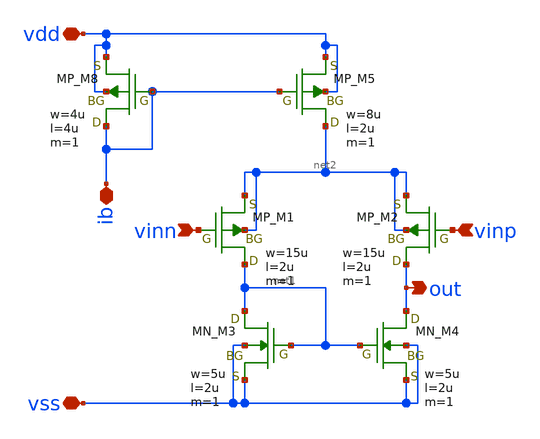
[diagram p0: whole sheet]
** sch_path: member_project/DCDC/xschem/diff.sch
**.subckt diff vdd vss vinn vinp out ib
*.iopin vdd
*.iopin vss
*.ipin vinn
*.ipin vinp
*.opin out
*.iopin ib
XM1 net1 vinn net2 net2 PMOS w=15u l=2u as=0 ad=0 ps=0 pd=0 nrd=0 nrs=0 m=1
XM2 out vinp net2 net2 PMOS w=15u l=2u as=0 ad=0 ps=0 pd=0 nrd=0 nrs=0 m=1
XM3 net1 net1 vss vss NMOS w=5u l=2u as=0 ad=0 ps=0 pd=0 nrd=0 nrs=0 m=1
XM4 out net1 vss vss NMOS w=5u l=2u as=0 ad=0 ps=0 pd=0 nrd=0 nrs=0 m=1
XM5 net2 ib vdd vdd PMOS w=8u l=2u as=0 ad=0 ps=0 pd=0 nrd=0 nrs=0 m=1
XM8 ib ib vdd vdd PMOS w=4u l=4u as=0 ad=0 ps=0 pd=0 nrd=0 nrs=0 m=1
**.ends
.end
